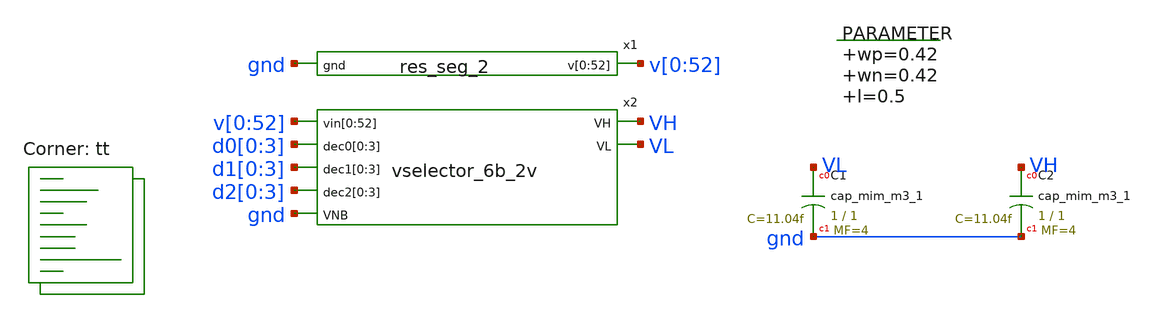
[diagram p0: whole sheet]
** sch_path: xschem/res_seg_2-tb.sch
**.subckt res_seg_2-tb
x1 v[0] v[1] v[2] v[3] v[4] v[5] v[6] v[7] v[8] v[9] v[10] v[11] v[12] v[13] v[14] v[15] v[16] v[17]
+ v[18] v[19] v[20] v[21] v[22] v[23] v[24] v[25] v[26] v[27] v[28] v[29] v[30] v[31] v[32] v[33] v[34]
+ v[35] v[36] v[37] v[38] v[39] v[40] v[41] v[42] v[43] v[44] v[45] v[46] v[47] v[48] v[49] v[50] v[51]
+ v[52] gnd res_seg_2
x2 v[0] v[1] v[2] v[3] v[4] v[5] v[6] v[7] v[8] v[9] v[10] v[11] v[12] v[13] v[14] v[15] v[16] v[17]
+ v[18] v[19] v[20] v[21] v[22] v[23] v[24] v[25] v[26] v[27] v[28] v[29] v[30] v[31] v[32] v[33] v[34]
+ v[35] v[36] v[37] v[38] v[39] v[40] v[41] v[42] v[43] v[44] v[45] v[46] v[47] v[48] v[49] v[50] v[51]
+ v[52] d0[0] d0[1] d0[2] d0[3] d1[0] d1[1] d1[2] d1[3] d2[0] d2[1] d2[2] d2[3] VH VL gnd vselector_6b_2v
.param wp=0.42 wn=0.42 l=0.5

XC1 VL gnd sky130_fd_pr__cap_mim_m3_1 W=1 L=1 MF=4 m=4
XC2 VH gnd sky130_fd_pr__cap_mim_m3_1 W=1 L=1 MF=4 m=4
**** begin user architecture code
.lib $::SKYWATER_MODELS/sky130.lib.spice tt



  .option wnflag=1
  .option safecurrents
  .options reltol=1e-5
  ********************Static Voltage Sources***************************
  Vddh vddh gnd dc 5.5

  V52 v[52] gnd dc 4.3209
  v0 v[0] gnd dc 1.0442
  ********************Dynamic Voltage Sources***************************
  *******Calculation**********
  .param base_f=100e3 base_t={1/base_f} base_th={base_t/2} base_d={base_th}
  .param d2_th ={base_th} d2_t={d1_th}
  .param d1_th ={4*d2_th} d1_t={d0_th}
  .param d0_th ={4*d1_th} d0_t={4*d0_th}

  .param d20_d ={0} d21_d={1*d2_th} d22_d={2*d2_th} d23_d={3*d2_th}
  .param d10_d ={0} d11_d={1*d1_th} d12_d={2*d1_th} d13_d={3*d1_th}
  .param d00_d ={0} d01_d={1*d0_th} d02_d={2*d0_th} d03_d={3*d0_th}
  *******Signals**********
  .param vhi=5.5
  Vd00 d0[0] gnd pulse(0 {vhi} {d00_d} 1n 1n {d0_th} {d0_t})
  Vd01 d0[1] gnd pulse(0 {vhi} {d01_d} 1n 1n {d0_th} {d0_t})
  Vd02 d0[2] gnd pulse(0 {vhi} {d02_d} 1n 1n {d0_th} {d0_t})
  Vd03 d0[3] gnd pulse(0 {vhi} {d03_d} 1n 1n {d0_th} {d0_t})

  Vd10 d1[0] gnd pulse(0 {vhi} {d10_d} 1n 1n {d1_th} {d1_t})
  Vd11 d1[1] gnd pulse(0 {vhi} {d11_d} 1n 1n {d1_th} {d1_t})
  Vd12 d1[2] gnd pulse(0 {vhi} {d12_d} 1n 1n {d1_th} {d1_t})
  Vd13 d1[3] gnd pulse(0 {vhi} {d13_d} 1n 1n {d1_th} {d1_t})

  Vd20 d2[0] gnd pulse(0 {vhi} {d20_d} 1n 1n {d2_th} {d2_t})
  Vd21 d2[1] gnd pulse(0 {vhi} {d21_d} 1n 1n {d2_th} {d2_t})
  Vd22 d2[2] gnd pulse(0 {vhi} {d22_d} 1n 1n {d2_th} {d2_t})
  Vd23 d2[3] gnd pulse(0 {vhi} {d23_d} 1n 1n {d2_th} {d2_t})
  ********************Simulation Commands*****************************
  .control
     reset
     save all
     tran 10n 500u
     write res_seg_2-tb.raw
     set appendwrite
*    quit 0
  .endc



**** end user architecture code
**.ends

* expanding   symbol:  res_seg_2.sym # of pins=2
** sym_path: xschem/res_seg_2.sym
** sch_path: xschem/res_seg_2.sch
.subckt res_seg_2 v[0] v[1] v[2] v[3] v[4] v[5] v[6] v[7] v[8] v[9] v[10] v[11] v[12] v[13] v[14]
+ v[15] v[16] v[17] v[18] v[19] v[20] v[21] v[22] v[23] v[24] v[25] v[26] v[27] v[28] v[29] v[30] v[31]
+ v[32] v[33] v[34] v[35] v[36] v[37] v[38] v[39] v[40] v[41] v[42] v[43] v[44] v[45] v[46] v[47] v[48]
+ v[49] v[50] v[51] v[52] gnd
*.opin
*+ v[0],v[1],v[2],v[3],v[4],v[5],v[6],v[7],v[8],v[9],v[10],v[11],v[12],v[13],v[14],v[15],v[16],v[17],v[18],v[19],v[20],v[21],v[22],v[23],v[24],v[25],v[26],v[27],v[28],v[29],v[30],v[31],v[32],v[33],v[34],v[35],v[36],v[37],v[38],v[39],v[40],v[41],v[42],v[43],v[44],v[45],v[46],v[47],v[48],v[49],v[50],v[51],v[52]
*.ipin gnd
XR1 v[1] v[0] gnd sky130_fd_pr__res_xhigh_po_0p35 L=2.1527 mult=1 m=1
XR2 v[2] v[1] gnd sky130_fd_pr__res_xhigh_po_0p35 L=1.9083 mult=1 m=1
XR3 v[3] v[2] gnd sky130_fd_pr__res_xhigh_po_0p35 L=1.7203 mult=1 m=1
XR4 v[4] v[3] gnd sky130_fd_pr__res_xhigh_po_0p35 L=1.5887 mult=1 m=1
XR5 v[5] v[4] gnd sky130_fd_pr__res_xhigh_po_0p35 L=1.4759 mult=1 m=1
XR6 v[6] v[5] gnd sky130_fd_pr__res_xhigh_po_0p35 L=1.3912 mult=1 m=1
XR7 v[7] v[6] gnd sky130_fd_pr__res_xhigh_po_0p35 L=1.316 mult=1 m=1
XR8 v[8] v[7] gnd sky130_fd_pr__res_xhigh_po_0p35 L=1.2502 mult=1 m=1
XR9 v[9] v[8] gnd sky130_fd_pr__res_xhigh_po_0p35 L=1.1938 mult=1 m=1
XR10 v[10] v[9] gnd sky130_fd_pr__res_xhigh_po_0p35 L=1.1562 mult=1 m=1
XR11 v[11] v[10] gnd sky130_fd_pr__res_xhigh_po_0p35 L=1.1186 mult=1 m=1
XR12 v[12] v[11] gnd sky130_fd_pr__res_xhigh_po_0p35 L=1.081 mult=1 m=1
XR13 v[13] v[12] gnd sky130_fd_pr__res_xhigh_po_0p35 L=1.0528 mult=1 m=1
XR14 v[14] v[13] gnd sky130_fd_pr__res_xhigh_po_0p35 L=1.034 mult=1 m=1
XR15 v[15] v[14] gnd sky130_fd_pr__res_xhigh_po_0p35 L=1.0058 mult=1 m=1
XR16 v[16] v[15] gnd sky130_fd_pr__res_xhigh_po_0p35 L=0.9776 mult=1 m=1
XR17 v[17] v[16] gnd sky130_fd_pr__res_xhigh_po_0p35 L=0.9682 mult=1 m=1
XR18 v[18] v[17] gnd sky130_fd_pr__res_xhigh_po_0p35 L=0.9588 mult=1 m=1
XR19 v[19] v[18] gnd sky130_fd_pr__res_xhigh_po_0p35 L=0.94 mult=1 m=1
XR20 v[20] v[19] gnd sky130_fd_pr__res_xhigh_po_0p35 L=0.9212 mult=1 m=1
XR22 v[22] v[21] gnd sky130_fd_pr__res_xhigh_po_0p35 L=0.9118 mult=1 m=1
XR23 v[23] v[22] gnd sky130_fd_pr__res_xhigh_po_0p35 L=0.9024 mult=1 m=1
XR24 v[24] v[23] gnd sky130_fd_pr__res_xhigh_po_0p35 L=0.893 mult=1 m=1
XR27 v[27] v[26] gnd sky130_fd_pr__res_xhigh_po_0p35 L=0.8836 mult=1 m=1
XR33 v[33] v[32] gnd sky130_fd_pr__res_xhigh_po_0p35 L=0.9024 mult=1 m=1
XR35 v[35] v[34] gnd sky130_fd_pr__res_xhigh_po_0p35 L=0.9118 mult=1 m=1
XR36 v[36] v[35] gnd sky130_fd_pr__res_xhigh_po_0p35 L=0.9212 mult=1 m=1
XR38 v[38] v[37] gnd sky130_fd_pr__res_xhigh_po_0p35 L=0.9494 mult=1 m=1
XR40 v[40] v[39] gnd sky130_fd_pr__res_xhigh_po_0p35 L=0.9776 mult=1 m=1
XR41 v[41] v[40] gnd sky130_fd_pr__res_xhigh_po_0p35 L=0.987 mult=1 m=1
XR42 v[42] v[41] gnd sky130_fd_pr__res_xhigh_po_0p35 L=1.0058 mult=1 m=1
XR43 v[43] v[42] gnd sky130_fd_pr__res_xhigh_po_0p35 L=1.034 mult=1 m=1
XR44 v[44] v[43] gnd sky130_fd_pr__res_xhigh_po_0p35 L=1.0528 mult=1 m=1
XR45 v[45] v[44] gnd sky130_fd_pr__res_xhigh_po_0p35 L=1.081 mult=1 m=1
XR46 v[46] v[45] gnd sky130_fd_pr__res_xhigh_po_0p35 L=1.1092 mult=1 m=1
XR47 v[47] v[46] gnd sky130_fd_pr__res_xhigh_po_0p35 L=1.1468 mult=1 m=1
XR48 v[48] v[47] gnd sky130_fd_pr__res_xhigh_po_0p35 L=1.1938 mult=1 m=1
XR49 v[49] v[48] gnd sky130_fd_pr__res_xhigh_po_0p35 L=1.2408 mult=1 m=1
XR50 v[50] v[49] gnd sky130_fd_pr__res_xhigh_po_0p35 L=1.2878 mult=1 m=1
XR51 v[51] v[50] gnd sky130_fd_pr__res_xhigh_po_0p35 L=1.363 mult=1 m=1
XR52 v[52] v[51] gnd sky130_fd_pr__res_xhigh_po_0p35 L=1.4383 mult=1 m=1
XR28 v[28] v[27] gnd sky130_fd_pr__res_xhigh_po_0p35 L=0.893 mult=1 m=1
XR29 v[29] v[28] gnd sky130_fd_pr__res_xhigh_po_0p35 L=0.8836 mult=1 m=1
XR37 v[37] v[36] gnd sky130_fd_pr__res_xhigh_po_0p35 L=0.9306 mult=1 m=1
XR21 v[21] v[20] gnd sky130_fd_pr__res_xhigh_po_0p35 L=0.9212 mult=1 m=1
XR25 v[25] v[24] gnd sky130_fd_pr__res_xhigh_po_0p35 L=0.893 mult=1 m=1
XR26 v[26] v[25] gnd sky130_fd_pr__res_xhigh_po_0p35 L=0.893 mult=1 m=1
XR30 v[30] v[29] gnd sky130_fd_pr__res_xhigh_po_0p35 L=0.8836 mult=1 m=1
XR31 v[31] v[30] gnd sky130_fd_pr__res_xhigh_po_0p35 L=0.893 mult=1 m=1
XR32 v[32] v[31] gnd sky130_fd_pr__res_xhigh_po_0p35 L=0.893 mult=1 m=1
XR34 v[34] v[33] gnd sky130_fd_pr__res_xhigh_po_0p35 L=0.9024 mult=1 m=1
XR39 v[39] v[38] gnd sky130_fd_pr__res_xhigh_po_0p35 L=0.9494 mult=1 m=1
.ends


* expanding   symbol:  vselector_6b_2v.sym # of pins=7
** sym_path: xschem/vselector_6b_2v.sym
** sch_path: xschem/vselector_6b_2v.sch
.subckt vselector_6b_2v vin[0] vin[1] vin[2] vin[3] vin[4] vin[5] vin[6] vin[7] vin[8] vin[9]
+ vin[10] vin[11] vin[12] vin[13] vin[14] vin[15] vin[16] vin[17] vin[18] vin[19] vin[20] vin[21] vin[22]
+ vin[23] vin[24] vin[25] vin[26] vin[27] vin[28] vin[29] vin[30] vin[31] vin[32] vin[33] vin[34] vin[35]
+ vin[36] vin[37] vin[38] vin[39] vin[40] vin[41] vin[42] vin[43] vin[44] vin[45] vin[46] vin[47] vin[48]
+ vin[49] vin[50] vin[51] vin[52] dec0[0] dec0[1] dec0[2] dec0[3] dec1[0] dec1[1] dec1[2] dec1[3] dec2[0]
+ dec2[1] dec2[2] dec2[3] VH VL VNB
*.ipin
*+ vin[0],vin[1],vin[2],vin[3],vin[4],vin[5],vin[6],vin[7],vin[8],vin[9],vin[10],vin[11],vin[12],vin[13],vin[14],vin[15],vin[16],vin[17],vin[18],vin[19],vin[20],vin[21],vin[22],vin[23],vin[24],vin[25],vin[26],vin[27],vin[28],vin[29],vin[30],vin[31],vin[32],vin[33],vin[34],vin[35],vin[36],vin[37],vin[38],vin[39],vin[40],vin[41],vin[42],vin[43],vin[44],vin[45],vin[46],vin[47],vin[48],vin[49],vin[50],vin[51],vin[52]
*.opin VH
*.ipin VNB
*.ipin dec0[0],dec0[1],dec0[2],dec0[3]
*.opin VL
*.ipin dec1[0],dec1[1],dec1[2],dec1[3]
*.ipin dec2[0],dec2[1],dec2[2],dec2[3]
x1 vin[0] vin[1] vin[2] vin[3] vin[4] vin[5] vin[6] vin[7] vin[8] vin[9] vin[10] vin[11] vin[12]
+ vin[13] vin[14] vin[15] vin[16] vin[17] vin[18] vin[19] vin[20] vin[21] vin[22] vin[23] vin[24] vin[25]
+ vin[26] vin[27] vin[28] vin[29] vin[30] vin[31] vin[32] vin[33] vin[34] vin[35] vin[36] vin[37] vin[38]
+ vin[39] vin[40] vin[41] vin[42] vin[43] vin[44] vin[45] vin[46] vin[47] vin[48] vin[49] vin[50] vin[51]
+ vin[52] dec0[0] dec0[1] dec0[2] dec0[3] dec0[0] vout1[0] vout1[1] vout1[2] vout1[3] vout1[4] vout1[5]
+ vout1[6] vout1[7] vout1[8] vout1[9] vout1[10] vout1[11] vout1[12] vout1[13] vout1[14] vout1[15] vout1[16]
+ VNB vselector_6b_2v_stage_1
x2 vout1[0] vout1[1] vout1[2] vout1[3] vout1[4] vout1[5] vout1[6] vout1[7] vout1[8] vout1[9]
+ vout1[10] vout1[11] vout1[12] vout1[13] vout1[14] vout1[15] vout1[16] dec1[0] dec1[1] dec1[2] dec1[3]
+ vout2[0] vout2[1] vout2[2] vout2[3] vout2[4] VNB vselector_6b_2v_stage_2
x3 vout2[0] vout2[1] vout2[2] vout2[3] vout2[4] dec2[0] dec2[1] dec2[2] dec2[3] VH VL VNB
+ vselector_6b_2v_stage_3
XC1 VL VNB sky130_fd_pr__cap_mim_m3_1 W=1 L=1 MF=8 m=8
XC2 VH VNB sky130_fd_pr__cap_mim_m3_1 W=1 L=1 MF=8 m=8
.ends


* expanding   symbol:  vselector_6b_2v_stage_1.sym # of pins=4
** sym_path: xschem/vselector_6b_2v_stage_1.sym
** sch_path: xschem/vselector_6b_2v_stage_1.sch
.subckt vselector_6b_2v_stage_1 vin[0] vin[1] vin[2] vin[3] vin[4] vin[5] vin[6] vin[7] vin[8]
+ vin[9] vin[10] vin[11] vin[12] vin[13] vin[14] vin[15] vin[16] vin[17] vin[18] vin[19] vin[20] vin[21]
+ vin[22] vin[23] vin[24] vin[25] vin[26] vin[27] vin[28] vin[29] vin[30] vin[31] vin[32] vin[33] vin[34]
+ vin[35] vin[36] vin[37] vin[38] vin[39] vin[40] vin[41] vin[42] vin[43] vin[44] vin[45] vin[46] vin[47]
+ vin[48] vin[49] vin[50] vin[51] vin[52] dec[0] dec[1] dec[2] dec[3] dec[4] vout[0] vout[1] vout[2] vout[3]
+ vout[4] vout[5] vout[6] vout[7] vout[8] vout[9] vout[10] vout[11] vout[12] vout[13] vout[14] vout[15]
+ vout[16] VNB
*.ipin
*+ vin[0],vin[1],vin[2],vin[3],vin[4],vin[5],vin[6],vin[7],vin[8],vin[9],vin[10],vin[11],vin[12],vin[13],vin[14],vin[15],vin[16],vin[17],vin[18],vin[19],vin[20],vin[21],vin[22],vin[23],vin[24],vin[25],vin[26],vin[27],vin[28],vin[29],vin[30],vin[31],vin[32],vin[33],vin[34],vin[35],vin[36],vin[37],vin[38],vin[39],vin[40],vin[41],vin[42],vin[43],vin[44],vin[45],vin[46],vin[47],vin[48],vin[49],vin[50],vin[51],vin[52]
*.opin
*+ vout[0],vout[1],vout[2],vout[3],vout[4],vout[5],vout[6],vout[7],vout[8],vout[9],vout[10],vout[11],vout[12],vout[13],vout[14],vout[15],vout[16]
*.ipin VNB
*.ipin dec[0],dec[1],dec[2],dec[3],dec[4]
x1 vin[0] vin[1] vin[2] vin[3] vin[4] vin[5] vin[6] vin[7] vin[8] vin[9] vin[10] vin[11] vin[12]
+ vin[13] vin[14] vin[15] vin[16] dec[0] vout[0] vout[1] vout[2] vout[3] vout[4] vout[5] vout[6] vout[7]
+ vout[8] vout[9] vout[10] vout[11] vout[12] vout[13] vout[14] vout[15] vout[16] VNB vselector_16b
x2 vin[16] vin[17] vin[18] vin[19] vin[20] vin[21] vin[22] vin[23] vin[24] vin[25] vin[26] vin[27]
+ vin[28] vin[29] vin[30] vin[31] vin[32] dec[1] vout[0] vout[1] vout[2] vout[3] vout[4] vout[5] vout[6]
+ vout[7] vout[8] vout[9] vout[10] vout[11] vout[12] vout[13] vout[14] vout[15] vout[16] VNB vselector_16b
x3 vin[32] vin[33] vin[34] vin[35] vin[36] vin[37] vin[38] vin[39] vin[40] vin[41] vin[42] vin[43]
+ vin[44] vin[45] vin[46] vin[47] vin[48] dec[2] vout[0] vout[1] vout[2] vout[3] vout[4] vout[5] vout[6]
+ vout[7] vout[8] vout[9] vout[10] vout[11] vout[12] vout[13] vout[14] vout[15] vout[16] VNB vselector_16b
x4 vin[48] vin[49] vin[50] vin[51] vin[52] dec[3] vout[0] vout[1] vout[2] vout[3] vout[4] VNB
+ vselector_4b
.ends


* expanding   symbol:  vselector_6b_2v_stage_2.sym # of pins=4
** sym_path: xschem/vselector_6b_2v_stage_2.sym
** sch_path: xschem/vselector_6b_2v_stage_2.sch
.subckt vselector_6b_2v_stage_2 vin[0] vin[1] vin[2] vin[3] vin[4] vin[5] vin[6] vin[7] vin[8]
+ vin[9] vin[10] vin[11] vin[12] vin[13] vin[14] vin[15] vin[16] dec[0] dec[1] dec[2] dec[3] vout[0] vout[1]
+ vout[2] vout[3] vout[4] VNB
*.ipin
*+ vin[0],vin[1],vin[2],vin[3],vin[4],vin[5],vin[6],vin[7],vin[8],vin[9],vin[10],vin[11],vin[12],vin[13],vin[14],vin[15],vin[16]
*.opin vout[0],vout[1],vout[2],vout[3],vout[4]
*.ipin VNB
*.ipin dec[0],dec[1],dec[2],dec[3]
x1 vin[0] vin[1] vin[2] vin[3] vin[4] dec[0] vout[0] vout[1] vout[2] vout[3] vout[4] VNB
+ vselector_4b
x2 vin[4] vin[5] vin[6] vin[7] vin[8] dec[1] vout[0] vout[1] vout[2] vout[3] vout[4] VNB
+ vselector_4b
x3 vin[8] vin[9] vin[10] vin[11] vin[12] dec[2] vout[0] vout[1] vout[2] vout[3] vout[4] VNB
+ vselector_4b
x4 vin[12] vin[13] vin[14] vin[15] vin[16] dec[3] vout[0] vout[1] vout[2] vout[3] vout[4] VNB
+ vselector_4b
.ends


* expanding   symbol:  vselector_6b_2v_stage_3.sym # of pins=5
** sym_path: xschem/vselector_6b_2v_stage_3.sym
** sch_path: xschem/vselector_6b_2v_stage_3.sch
.subckt vselector_6b_2v_stage_3 vin[0] vin[1] vin[2] vin[3] vin[4] dec[0] dec[1] dec[2] dec[3] VH VL
+ VNB
*.ipin vin[0],vin[1],vin[2],vin[3],vin[4]
*.opin VH
*.ipin VNB
*.ipin dec[0],dec[1],dec[2],dec[3]
*.opin VL
x1 vin[0] vin[1] dec[0] VH VL VNB vselector_1b
x2 vin[1] vin[2] dec[1] VH VL VNB vselector_1b
x3 vin[2] vin[3] dec[2] VH VL VNB vselector_1b
x4 vin[3] vin[4] dec[3] VH VL VNB vselector_1b
.ends


* expanding   symbol:  vselector_16b.sym # of pins=4
** sym_path: xschem/vselector_16b.sym
** sch_path: xschem/vselector_16b.sch
.subckt vselector_16b vin[0] vin[1] vin[2] vin[3] vin[4] vin[5] vin[6] vin[7] vin[8] vin[9] vin[10]
+ vin[11] vin[12] vin[13] vin[14] vin[15] vin[16] DIN vout[0] vout[1] vout[2] vout[3] vout[4] vout[5] vout[6]
+ vout[7] vout[8] vout[9] vout[10] vout[11] vout[12] vout[13] vout[14] vout[15] vout[16] VNB
*.ipin
*+ vin[0],vin[1],vin[2],vin[3],vin[4],vin[5],vin[6],vin[7],vin[8],vin[9],vin[10],vin[11],vin[12],vin[13],vin[14],vin[15],vin[16]
*.opin
*+ vout[0],vout[1],vout[2],vout[3],vout[4],vout[5],vout[6],vout[7],vout[8],vout[9],vout[10],vout[11],vout[12],vout[13],vout[14],vout[15],vout[16]
*.ipin VNB
*.ipin DIN
XM1 vout[0] DIN vin[0] VNB sky130_fd_pr__nfet_g5v0d10v5 L=l W=wn nf=1 ad='int((nf+1)/2) * W/nf * 0.29'
+ as='int((nf+2)/2) * W/nf * 0.29' pd='2*int((nf+1)/2) * (W/nf + 0.29)' ps='2*int((nf+2)/2) * (W/nf + 0.29)'
+ nrd='0.29 / W' nrs='0.29 / W' sa=0 sb=0 sd=0 mult=1 m=1
XM2 vout[1] DIN vin[1] VNB sky130_fd_pr__nfet_g5v0d10v5 L=l W=wn nf=1 ad='int((nf+1)/2) * W/nf * 0.29'
+ as='int((nf+2)/2) * W/nf * 0.29' pd='2*int((nf+1)/2) * (W/nf + 0.29)' ps='2*int((nf+2)/2) * (W/nf + 0.29)'
+ nrd='0.29 / W' nrs='0.29 / W' sa=0 sb=0 sd=0 mult=1 m=1
XM3 vout[2] DIN vin[2] VNB sky130_fd_pr__nfet_g5v0d10v5 L=l W=wn nf=1 ad='int((nf+1)/2) * W/nf * 0.29'
+ as='int((nf+2)/2) * W/nf * 0.29' pd='2*int((nf+1)/2) * (W/nf + 0.29)' ps='2*int((nf+2)/2) * (W/nf + 0.29)'
+ nrd='0.29 / W' nrs='0.29 / W' sa=0 sb=0 sd=0 mult=1 m=1
XM4 vout[3] DIN vin[3] VNB sky130_fd_pr__nfet_g5v0d10v5 L=l W=wn nf=1 ad='int((nf+1)/2) * W/nf * 0.29'
+ as='int((nf+2)/2) * W/nf * 0.29' pd='2*int((nf+1)/2) * (W/nf + 0.29)' ps='2*int((nf+2)/2) * (W/nf + 0.29)'
+ nrd='0.29 / W' nrs='0.29 / W' sa=0 sb=0 sd=0 mult=1 m=1
XM5 vout[4] DIN vin[4] VNB sky130_fd_pr__nfet_g5v0d10v5 L=l W=wn nf=1 ad='int((nf+1)/2) * W/nf * 0.29'
+ as='int((nf+2)/2) * W/nf * 0.29' pd='2*int((nf+1)/2) * (W/nf + 0.29)' ps='2*int((nf+2)/2) * (W/nf + 0.29)'
+ nrd='0.29 / W' nrs='0.29 / W' sa=0 sb=0 sd=0 mult=1 m=1
XM6 vout[5] DIN vin[5] VNB sky130_fd_pr__nfet_g5v0d10v5 L=l W=wn nf=1 ad='int((nf+1)/2) * W/nf * 0.29'
+ as='int((nf+2)/2) * W/nf * 0.29' pd='2*int((nf+1)/2) * (W/nf + 0.29)' ps='2*int((nf+2)/2) * (W/nf + 0.29)'
+ nrd='0.29 / W' nrs='0.29 / W' sa=0 sb=0 sd=0 mult=1 m=1
XM7 vout[6] DIN vin[6] VNB sky130_fd_pr__nfet_g5v0d10v5 L=l W=wn nf=1 ad='int((nf+1)/2) * W/nf * 0.29'
+ as='int((nf+2)/2) * W/nf * 0.29' pd='2*int((nf+1)/2) * (W/nf + 0.29)' ps='2*int((nf+2)/2) * (W/nf + 0.29)'
+ nrd='0.29 / W' nrs='0.29 / W' sa=0 sb=0 sd=0 mult=1 m=1
XM8 vout[7] DIN vin[7] VNB sky130_fd_pr__nfet_g5v0d10v5 L=l W=wn nf=1 ad='int((nf+1)/2) * W/nf * 0.29'
+ as='int((nf+2)/2) * W/nf * 0.29' pd='2*int((nf+1)/2) * (W/nf + 0.29)' ps='2*int((nf+2)/2) * (W/nf + 0.29)'
+ nrd='0.29 / W' nrs='0.29 / W' sa=0 sb=0 sd=0 mult=1 m=1
XM9 vout[8] DIN vin[8] VNB sky130_fd_pr__nfet_g5v0d10v5 L=l W=wn nf=1 ad='int((nf+1)/2) * W/nf * 0.29'
+ as='int((nf+2)/2) * W/nf * 0.29' pd='2*int((nf+1)/2) * (W/nf + 0.29)' ps='2*int((nf+2)/2) * (W/nf + 0.29)'
+ nrd='0.29 / W' nrs='0.29 / W' sa=0 sb=0 sd=0 mult=1 m=1
XM10 vout[9] DIN vin[9] VNB sky130_fd_pr__nfet_g5v0d10v5 L=l W=wn nf=1 ad='int((nf+1)/2) * W/nf * 0.29'
+ as='int((nf+2)/2) * W/nf * 0.29' pd='2*int((nf+1)/2) * (W/nf + 0.29)' ps='2*int((nf+2)/2) * (W/nf + 0.29)'
+ nrd='0.29 / W' nrs='0.29 / W' sa=0 sb=0 sd=0 mult=1 m=1
XM11 vout[10] DIN vin[10] VNB sky130_fd_pr__nfet_g5v0d10v5 L=l W=wn nf=1 ad='int((nf+1)/2) * W/nf * 0.29'
+ as='int((nf+2)/2) * W/nf * 0.29' pd='2*int((nf+1)/2) * (W/nf + 0.29)' ps='2*int((nf+2)/2) * (W/nf + 0.29)'
+ nrd='0.29 / W' nrs='0.29 / W' sa=0 sb=0 sd=0 mult=1 m=1
XM12 vout[11] DIN vin[11] VNB sky130_fd_pr__nfet_g5v0d10v5 L=l W=wn nf=1 ad='int((nf+1)/2) * W/nf * 0.29'
+ as='int((nf+2)/2) * W/nf * 0.29' pd='2*int((nf+1)/2) * (W/nf + 0.29)' ps='2*int((nf+2)/2) * (W/nf + 0.29)'
+ nrd='0.29 / W' nrs='0.29 / W' sa=0 sb=0 sd=0 mult=1 m=1
XM13 vout[12] DIN vin[12] VNB sky130_fd_pr__nfet_g5v0d10v5 L=l W=wn nf=1 ad='int((nf+1)/2) * W/nf * 0.29'
+ as='int((nf+2)/2) * W/nf * 0.29' pd='2*int((nf+1)/2) * (W/nf + 0.29)' ps='2*int((nf+2)/2) * (W/nf + 0.29)'
+ nrd='0.29 / W' nrs='0.29 / W' sa=0 sb=0 sd=0 mult=1 m=1
XM14 vout[13] DIN vin[13] VNB sky130_fd_pr__nfet_g5v0d10v5 L=l W=wn nf=1 ad='int((nf+1)/2) * W/nf * 0.29'
+ as='int((nf+2)/2) * W/nf * 0.29' pd='2*int((nf+1)/2) * (W/nf + 0.29)' ps='2*int((nf+2)/2) * (W/nf + 0.29)'
+ nrd='0.29 / W' nrs='0.29 / W' sa=0 sb=0 sd=0 mult=1 m=1
XM15 vout[14] DIN vin[14] VNB sky130_fd_pr__nfet_g5v0d10v5 L=l W=wn nf=1 ad='int((nf+1)/2) * W/nf * 0.29'
+ as='int((nf+2)/2) * W/nf * 0.29' pd='2*int((nf+1)/2) * (W/nf + 0.29)' ps='2*int((nf+2)/2) * (W/nf + 0.29)'
+ nrd='0.29 / W' nrs='0.29 / W' sa=0 sb=0 sd=0 mult=1 m=1
XM16 vout[15] DIN vin[15] VNB sky130_fd_pr__nfet_g5v0d10v5 L=l W=wn nf=1 ad='int((nf+1)/2) * W/nf * 0.29'
+ as='int((nf+2)/2) * W/nf * 0.29' pd='2*int((nf+1)/2) * (W/nf + 0.29)' ps='2*int((nf+2)/2) * (W/nf + 0.29)'
+ nrd='0.29 / W' nrs='0.29 / W' sa=0 sb=0 sd=0 mult=1 m=1
XM17 vout[16] DIN vin[16] VNB sky130_fd_pr__nfet_g5v0d10v5 L=l W=wn nf=1 ad='int((nf+1)/2) * W/nf * 0.29'
+ as='int((nf+2)/2) * W/nf * 0.29' pd='2*int((nf+1)/2) * (W/nf + 0.29)' ps='2*int((nf+2)/2) * (W/nf + 0.29)'
+ nrd='0.29 / W' nrs='0.29 / W' sa=0 sb=0 sd=0 mult=1 m=1
.ends


* expanding   symbol:  vselector_4b.sym # of pins=4
** sym_path: xschem/vselector_4b.sym
** sch_path: xschem/vselector_4b.sch
.subckt vselector_4b vin[0] vin[1] vin[2] vin[3] vin[4] DIN vout[0] vout[1] vout[2] vout[3] vout[4]
+ VNB
*.ipin vin[0],vin[1],vin[2],vin[3],vin[4]
*.opin vout[0],vout[1],vout[2],vout[3],vout[4]
*.ipin VNB
*.ipin DIN
XM1 vout[0] DIN vin[0] VNB sky130_fd_pr__nfet_g5v0d10v5 L=l W=wn nf=1 ad='int((nf+1)/2) * W/nf * 0.29'
+ as='int((nf+2)/2) * W/nf * 0.29' pd='2*int((nf+1)/2) * (W/nf + 0.29)' ps='2*int((nf+2)/2) * (W/nf + 0.29)'
+ nrd='0.29 / W' nrs='0.29 / W' sa=0 sb=0 sd=0 mult=1 m=1
XM2 vout[1] DIN vin[1] VNB sky130_fd_pr__nfet_g5v0d10v5 L=l W=wn nf=1 ad='int((nf+1)/2) * W/nf * 0.29'
+ as='int((nf+2)/2) * W/nf * 0.29' pd='2*int((nf+1)/2) * (W/nf + 0.29)' ps='2*int((nf+2)/2) * (W/nf + 0.29)'
+ nrd='0.29 / W' nrs='0.29 / W' sa=0 sb=0 sd=0 mult=1 m=1
XM3 vout[2] DIN vin[2] VNB sky130_fd_pr__nfet_g5v0d10v5 L=l W=wn nf=1 ad='int((nf+1)/2) * W/nf * 0.29'
+ as='int((nf+2)/2) * W/nf * 0.29' pd='2*int((nf+1)/2) * (W/nf + 0.29)' ps='2*int((nf+2)/2) * (W/nf + 0.29)'
+ nrd='0.29 / W' nrs='0.29 / W' sa=0 sb=0 sd=0 mult=1 m=1
XM4 vout[3] DIN vin[3] VNB sky130_fd_pr__nfet_g5v0d10v5 L=l W=wn nf=1 ad='int((nf+1)/2) * W/nf * 0.29'
+ as='int((nf+2)/2) * W/nf * 0.29' pd='2*int((nf+1)/2) * (W/nf + 0.29)' ps='2*int((nf+2)/2) * (W/nf + 0.29)'
+ nrd='0.29 / W' nrs='0.29 / W' sa=0 sb=0 sd=0 mult=1 m=1
XM5 vout[4] DIN vin[4] VNB sky130_fd_pr__nfet_g5v0d10v5 L=l W=wn nf=1 ad='int((nf+1)/2) * W/nf * 0.29'
+ as='int((nf+2)/2) * W/nf * 0.29' pd='2*int((nf+1)/2) * (W/nf + 0.29)' ps='2*int((nf+2)/2) * (W/nf + 0.29)'
+ nrd='0.29 / W' nrs='0.29 / W' sa=0 sb=0 sd=0 mult=1 m=1
.ends


* expanding   symbol:  vselector_1b.sym # of pins=5
** sym_path: xschem/vselector_1b.sym
** sch_path: xschem/vselector_1b.sch
.subckt vselector_1b vin[0] vin[1] DIN VH VL VNB
*.ipin vin[0],vin[1]
*.opin VL
*.ipin VNB
*.ipin DIN
*.opin VH
.param wp=0.42 wn=0.42 l=0.5

XM1 VL DIN vin[0] VNB sky130_fd_pr__nfet_g5v0d10v5 L=l W=wn nf=1 ad='int((nf+1)/2) * W/nf * 0.29' as='int((nf+2)/2) * W/nf * 0.29'
+ pd='2*int((nf+1)/2) * (W/nf + 0.29)' ps='2*int((nf+2)/2) * (W/nf + 0.29)' nrd='0.29 / W' nrs='0.29 / W'
+ sa=0 sb=0 sd=0 mult=1 m=1
XM2 VH DIN vin[1] VNB sky130_fd_pr__nfet_g5v0d10v5 L=l W=wn nf=1 ad='int((nf+1)/2) * W/nf * 0.29' as='int((nf+2)/2) * W/nf * 0.29'
+ pd='2*int((nf+1)/2) * (W/nf + 0.29)' ps='2*int((nf+2)/2) * (W/nf + 0.29)' nrd='0.29 / W' nrs='0.29 / W'
+ sa=0 sb=0 sd=0 mult=1 m=1
.ends

.end
